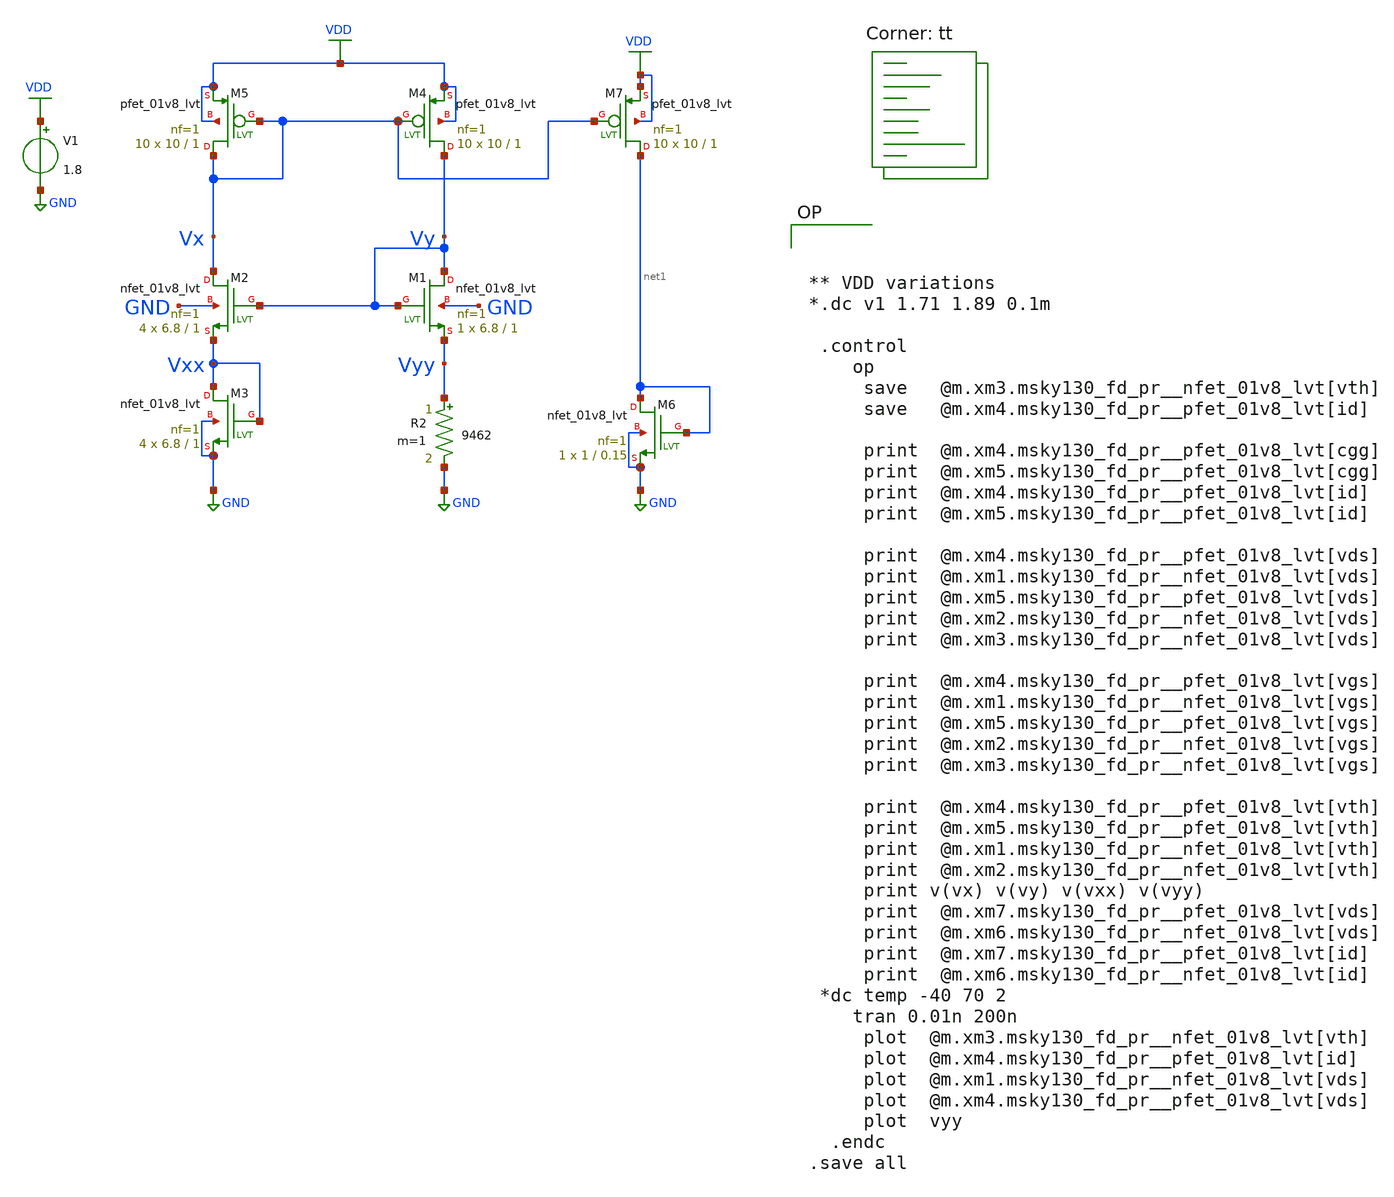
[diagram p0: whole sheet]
** sch_path: pll/lc_vco_lib_Hossam_Tarek/biasing_cct/xschem/constant_GM01.sch
**.subckt constant_GM01
XM1 Vy Vy Vyy GND sky130_fd_pr__nfet_01v8_lvt L=1 W=6.8 nf=1 ad='int((nf+1)/2) * W/nf * 0.29' as='int((nf+2)/2) * W/nf * 0.29'
+ pd='2*int((nf+1)/2) * (W/nf + 0.29)' ps='2*int((nf+2)/2) * (W/nf + 0.29)' nrd='0.29 / W' nrs='0.29 / W'
+ sa=0 sb=0 sd=0 mult=1 m=1
XM2 Vx Vy Vxx GND sky130_fd_pr__nfet_01v8_lvt L=1 W=6.8 nf=1 ad='int((nf+1)/2) * W/nf * 0.29' as='int((nf+2)/2) * W/nf * 0.29'
+ pd='2*int((nf+1)/2) * (W/nf + 0.29)' ps='2*int((nf+2)/2) * (W/nf + 0.29)' nrd='0.29 / W' nrs='0.29 / W'
+ sa=0 sb=0 sd=0 mult=4 m=4
XM3 Vxx Vxx GND GND sky130_fd_pr__nfet_01v8_lvt L=1 W=6.8 nf=1 ad='int((nf+1)/2) * W/nf * 0.29' as='int((nf+2)/2) * W/nf * 0.29'
+ pd='2*int((nf+1)/2) * (W/nf + 0.29)' ps='2*int((nf+2)/2) * (W/nf + 0.29)' nrd='0.29 / W' nrs='0.29 / W'
+ sa=0 sb=0 sd=0 mult=4 m=4
XM4 Vy Vx VDD VDD sky130_fd_pr__pfet_01v8_lvt L=1 W=10 nf=1 ad='int((nf+1)/2) * W/nf * 0.29' as='int((nf+2)/2) * W/nf * 0.29'
+ pd='2*int((nf+1)/2) * (W/nf + 0.29)' ps='2*int((nf+2)/2) * (W/nf + 0.29)' nrd='0.29 / W' nrs='0.29 / W'
+ sa=0 sb=0 sd=0 mult=10 m=10
XM5 Vx Vx VDD VDD sky130_fd_pr__pfet_01v8_lvt L=1 W=10 nf=1 ad='int((nf+1)/2) * W/nf * 0.29' as='int((nf+2)/2) * W/nf * 0.29'
+ pd='2*int((nf+1)/2) * (W/nf + 0.29)' ps='2*int((nf+2)/2) * (W/nf + 0.29)' nrd='0.29 / W' nrs='0.29 / W'
+ sa=0 sb=0 sd=0 mult=10 m=10
V1 VDD GND 1.8
R2 Vyy GND 9462 m=1
XM6 net1 net1 GND GND sky130_fd_pr__nfet_01v8_lvt L=0.15 W=1 nf=1 ad='int((nf+1)/2) * W/nf * 0.29' as='int((nf+2)/2) * W/nf * 0.29'
+ pd='2*int((nf+1)/2) * (W/nf + 0.29)' ps='2*int((nf+2)/2) * (W/nf + 0.29)' nrd='0.29 / W' nrs='0.29 / W'
+ sa=0 sb=0 sd=0 mult=1 m=1
XM7 net1 Vx VDD VDD sky130_fd_pr__pfet_01v8_lvt L=1 W=10 nf=1 ad='int((nf+1)/2) * W/nf * 0.29' as='int((nf+2)/2) * W/nf * 0.29'
+ pd='2*int((nf+1)/2) * (W/nf + 0.29)' ps='2*int((nf+2)/2) * (W/nf + 0.29)' nrd='0.29 / W' nrs='0.29 / W'
+ sa=0 sb=0 sd=0 mult=10 m=10
**** begin user architecture code



** VDD variations
*.dc v1 1.71 1.89 0.1m

 .control
    op
     save   @m.xm3.msky130_fd_pr__nfet_01v8_lvt[vth]
     save   @m.xm4.msky130_fd_pr__pfet_01v8_lvt[id]

     print  @m.xm4.msky130_fd_pr__pfet_01v8_lvt[cgg]
     print  @m.xm5.msky130_fd_pr__pfet_01v8_lvt[cgg]
     print  @m.xm4.msky130_fd_pr__pfet_01v8_lvt[id]
     print  @m.xm5.msky130_fd_pr__pfet_01v8_lvt[id]

     print  @m.xm4.msky130_fd_pr__pfet_01v8_lvt[vds]
     print  @m.xm1.msky130_fd_pr__nfet_01v8_lvt[vds]
     print  @m.xm5.msky130_fd_pr__pfet_01v8_lvt[vds]
     print  @m.xm2.msky130_fd_pr__nfet_01v8_lvt[vds]
     print  @m.xm3.msky130_fd_pr__nfet_01v8_lvt[vds]

     print  @m.xm4.msky130_fd_pr__pfet_01v8_lvt[vgs]
     print  @m.xm1.msky130_fd_pr__nfet_01v8_lvt[vgs]
     print  @m.xm5.msky130_fd_pr__pfet_01v8_lvt[vgs]
     print  @m.xm2.msky130_fd_pr__nfet_01v8_lvt[vgs]
     print  @m.xm3.msky130_fd_pr__nfet_01v8_lvt[vgs]

     print  @m.xm4.msky130_fd_pr__pfet_01v8_lvt[vth]
     print  @m.xm5.msky130_fd_pr__pfet_01v8_lvt[vth]
     print  @m.xm1.msky130_fd_pr__nfet_01v8_lvt[vth]
     print  @m.xm2.msky130_fd_pr__nfet_01v8_lvt[vth]
     print v(vx) v(vy) v(vxx) v(vyy)
     print  @m.xm7.msky130_fd_pr__pfet_01v8_lvt[vds]
     print  @m.xm6.msky130_fd_pr__nfet_01v8_lvt[vds]
     print  @m.xm7.msky130_fd_pr__pfet_01v8_lvt[id]
     print  @m.xm6.msky130_fd_pr__nfet_01v8_lvt[id]
 *dc temp -40 70 2
    tran 0.01n 200n
     plot  @m.xm3.msky130_fd_pr__nfet_01v8_lvt[vth]
     plot  @m.xm4.msky130_fd_pr__pfet_01v8_lvt[id]
     plot  @m.xm1.msky130_fd_pr__nfet_01v8_lvt[vds]
     plot  @m.xm4.msky130_fd_pr__pfet_01v8_lvt[vds]
     plot  vyy
  .endc
.save all

.lib $::SKYWATER_MODELS/sky130.lib.spice tt
**** end user architecture code
**.ends
.GLOBAL GND
.GLOBAL VDD
.end
